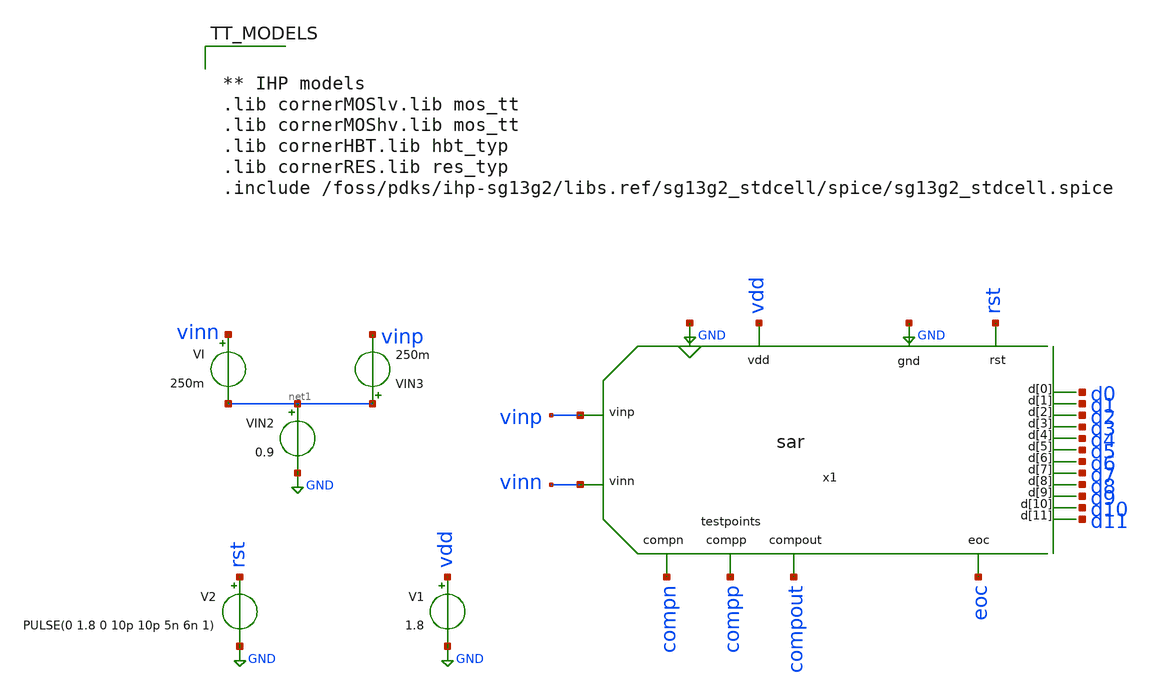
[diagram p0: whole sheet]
** sch_path: xschem/SAR_ADC/testbench/tb_sar_adc.sch
**.subckt tb_sar_adc
x1 vinp rst GND vinn GND vdd compn compp compout eoc d9 d7 d0 d11 d3 d4 d2 d1 d8 d6 d5 d10 sar
VI vinn net1 250m
V1 vdd GND 1.8
VIN2 net1 GND 0.9
VIN3 net1 vinp 250m
V2 rst GND PULSE(0 1.8 0 10p 10p 5n 6n 1)
**** begin user architecture code


.param period=5n
.param stoptime={18*period}
.param ro = 300
*.param stoptime=.2u
.options savecurrents klu method=gear reltol=1e-2 abstol=1e-15 gmin=1e-15
*vclk clk 0 PULSE(0 3.3 {0*period} {period*0.05} {period*0.05} {period/2} {period})
*vr  rst 0 PULSE(0 3.3 {0*period}  {period*0.05} {period*0.05} {period/2} {period} 1)

.tran {0.01*period} {stoptime}

.control
save all
run

plot {(V(d11)*2+V(d10)*4+V(d9)*8+V(d8)*16+V(d7)*32+V(d6)*64+V(d5)*128+V(d4)*256+V(d3)*512+V(d2)*1024+V(d1)*2048)/4095}
+ {2*rst} eoc {vinp - vinn}
plot {(-V(d0)*2048 + V(d1)*1024 + V(d2)*512 + V(d3)*256 + V(d4)*128 + V(d5)*64 + V(d6)*32 + V(d7)*16 + V(d8)*8 + V(d9)*4 + V(d10)*2 + V(d11))/2048}
plot compp compn {compout + 4}
plot {d0} {d1 + 4} {d2 + 8} {d3 + 12} {d4 + 16} {d5 + 20} {d6 + 24} {d7 + 28} {d8 + 32} {d9 + 36} {d10 + 40}
+ {d11 + 44} {x1.comp_clk + 50} {compout + 55} {eoc + 60}  {compp - compn - 2}

*plot d0
*plot d1
*plot d2
*plot d3
*plot d4
*plot d5
*plot d6
*plot d7
*plot d8
*plot d9
*plot d10
*plot d11
*plot compout
.endc




** IHP models
.lib cornerMOSlv.lib mos_tt
.lib cornerMOShv.lib mos_tt
.lib cornerHBT.lib hbt_typ
.lib cornerRES.lib res_typ
.include /foss/pdks/ihp-sg13g2/libs.ref/sg13g2_stdcell/spice/sg13g2_stdcell.spice


**** end user architecture code
**.ends
.GLOBAL GND
.end
